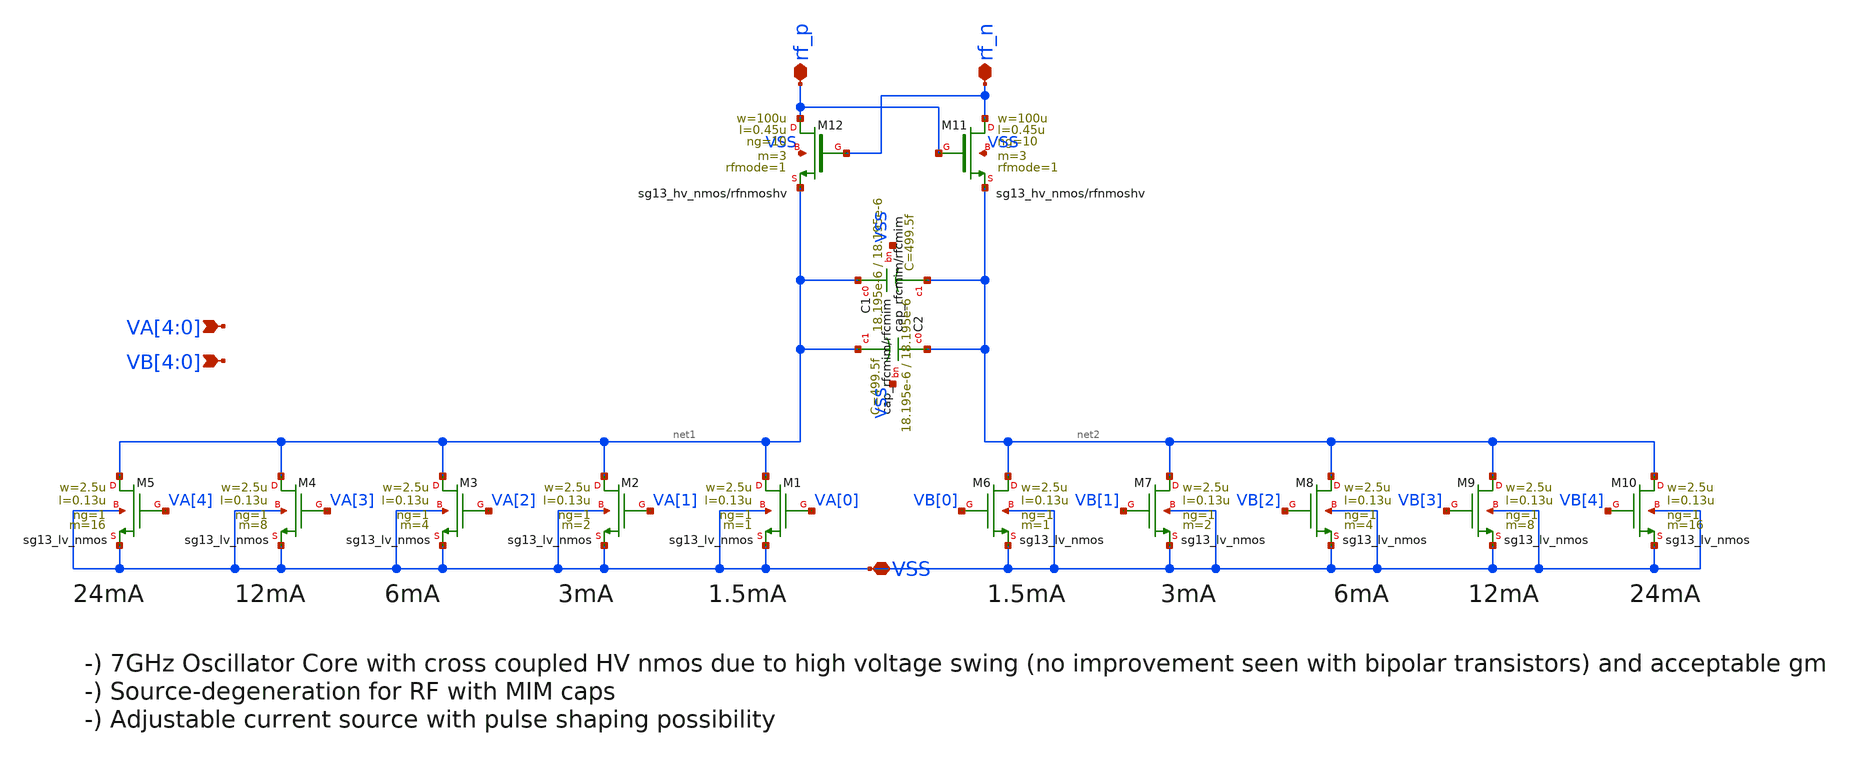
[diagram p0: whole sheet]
** sch_path: xschem/iruwbtx7_osci_core.sch
**.subckt iruwbtx7_osci_core rf_p rf_n VA[4],VA[3],VA[2],VA[1],VA[0] VB[4],VB[3],VB[2],VB[1],VB[0]
*+ VSS
*.iopin rf_p
*.iopin rf_n
*.ipin VA[4],VA[3],VA[2],VA[1],VA[0]
*.ipin VB[4],VB[3],VB[2],VB[1],VB[0]
*.iopin VSS
XM1 net1 VA[0] VSS VSS sg13_lv_nmos w=2.5u l=0.13u ng=1 m=1 mm_ok=1
XM2 net1 VA[1] VSS VSS sg13_lv_nmos w=2.5u l=0.13u ng=1 m=2 mm_ok=1
XM3 net1 VA[2] VSS VSS sg13_lv_nmos w=2.5u l=0.13u ng=1 m=4 mm_ok=1
XM4 net1 VA[3] VSS VSS sg13_lv_nmos w=2.5u l=0.13u ng=1 m=8 mm_ok=1
XM5 net1 VA[4] VSS VSS sg13_lv_nmos w=2.5u l=0.13u ng=1 m=16 mm_ok=1
XM6 net2 VB[0] VSS VSS sg13_lv_nmos w=2.5u l=0.13u ng=1 m=1 mm_ok=1
XM7 net2 VB[1] VSS VSS sg13_lv_nmos w=2.5u l=0.13u ng=1 m=2 mm_ok=1
XM8 net2 VB[2] VSS VSS sg13_lv_nmos w=2.5u l=0.13u ng=1 m=4 mm_ok=1
XM9 net2 VB[3] VSS VSS sg13_lv_nmos w=2.5u l=0.13u ng=1 m=8 mm_ok=1
XM10 net2 VB[4] VSS VSS sg13_lv_nmos w=2.5u l=0.13u ng=1 m=16 mm_ok=1
XC1 net1 net2 VSS cap_rfcmim w=18.195e-6 l=18.195e-6 wfeed=3.0e-6 m=1 mm_ok=1
XC2 net2 net1 VSS cap_rfcmim w=18.195e-6 l=18.195e-6 wfeed=3.0e-6 m=1 mm_ok=1
XM11 rf_n rf_p net2 VSS sg13_hv_nmos w=100u l=0.45u ng=10 m=3 rfmode=1 mm_ok=1
XM12 rf_p rf_n net1 VSS sg13_hv_nmos w=100u l=0.45u ng=10 m=3 rfmode=1 mm_ok=1
**.ends
.end
